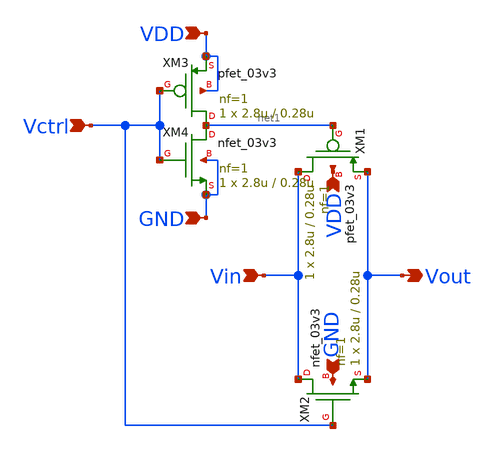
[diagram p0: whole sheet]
** sch_path: transmission-gate/sw_rc.sch
**.subckt sw_rc Vctrl Vin Vout VDD GND VDD GND
*.ipin Vctrl
*.ipin Vin
*.opin Vout
*.ipin VDD
*.ipin GND
*.ipin VDD
*.ipin GND
XM1 Vin net1 Vout VDD pfet_03v3 L=0.28u W=2.8u nf=1 ad='int((nf+1)/2) * W/nf * 0.18u' as='int((nf+2)/2) * W/nf * 0.18u'
+ pd='2*int((nf+1)/2) * (W/nf + 0.18u)' ps='2*int((nf+2)/2) * (W/nf + 0.18u)' nrd='0.18u / W' nrs='0.18u / W'
+ sa=0 sb=0 sd=0 m=1
XM2 Vin Vctrl Vout GND nfet_03v3 L=0.28u W=2.8u nf=1 ad='int((nf+1)/2) * W/nf * 0.18u' as='int((nf+2)/2) * W/nf * 0.18u'
+ pd='2*int((nf+1)/2) * (W/nf + 0.18u)' ps='2*int((nf+2)/2) * (W/nf + 0.18u)' nrd='0.18u / W' nrs='0.18u / W'
+ sa=0 sb=0 sd=0 m=1
XM3 net1 Vctrl VDD VDD pfet_03v3 L=0.28u W=2.8u nf=1 ad='int((nf+1)/2) * W/nf * 0.18u' as='int((nf+2)/2) * W/nf * 0.18u'
+ pd='2*int((nf+1)/2) * (W/nf + 0.18u)' ps='2*int((nf+2)/2) * (W/nf + 0.18u)' nrd='0.18u / W' nrs='0.18u / W'
+ sa=0 sb=0 sd=0 m=1
XM4 net1 Vctrl GND GND nfet_03v3 L=0.28u W=2.8u nf=1 ad='int((nf+1)/2) * W/nf * 0.18u' as='int((nf+2)/2) * W/nf * 0.18u'
+ pd='2*int((nf+1)/2) * (W/nf + 0.18u)' ps='2*int((nf+2)/2) * (W/nf + 0.18u)' nrd='0.18u / W' nrs='0.18u / W'
+ sa=0 sb=0 sd=0 m=1
**.ends
.end
